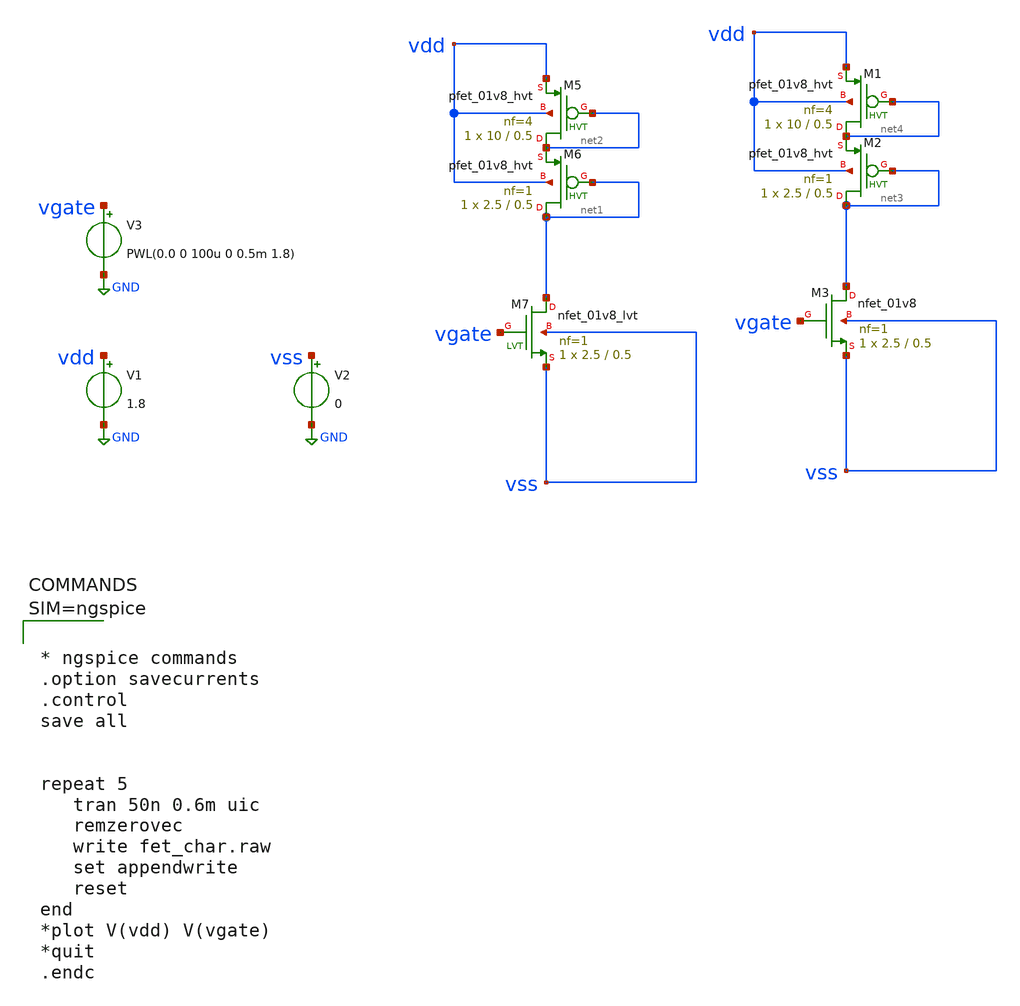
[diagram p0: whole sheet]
** sch_path: xschem/fet_char.sch
**.subckt fet_char
V1 vdd GND 1.8
V2 vss GND 0
XM5 net2 net2 vdd vdd sky130_fd_pr__pfet_01v8_hvt L=0.5 W=10 nf=4 ad='int((nf+1)/2) * W/nf * 0.29' as='int((nf+2)/2) * W/nf * 0.29'
+ pd='2*int((nf+1)/2) * (W/nf + 0.29)' ps='2*int((nf+2)/2) * (W/nf + 0.29)' nrd='0.29 / W' nrs='0.29 / W'
+ sa=0 sb=0 sd=0 mult=1 m=1
XM6 net1 net1 net2 vdd sky130_fd_pr__pfet_01v8_hvt L=0.5 W=2.5 nf=1 ad='int((nf+1)/2) * W/nf * 0.29'
+ as='int((nf+2)/2) * W/nf * 0.29' pd='2*int((nf+1)/2) * (W/nf + 0.29)' ps='2*int((nf+2)/2) * (W/nf + 0.29)'
+ nrd='0.29 / W' nrs='0.29 / W' sa=0 sb=0 sd=0 mult=1 m=1
XM7 net1 vgate vss vss sky130_fd_pr__nfet_01v8_lvt L=0.5 W=2.5 nf=1 ad='int((nf+1)/2) * W/nf * 0.29'
+ as='int((nf+2)/2) * W/nf * 0.29' pd='2*int((nf+1)/2) * (W/nf + 0.29)' ps='2*int((nf+2)/2) * (W/nf + 0.29)'
+ nrd='0.29 / W' nrs='0.29 / W' sa=0 sb=0 sd=0 mult=1 m=1
V3 vgate GND PWL(0.0 0 100u 0 0.5m 1.8)
XM1 net4 net4 vdd vdd sky130_fd_pr__pfet_01v8_hvt L=0.5 W=10 nf=4 ad='int((nf+1)/2) * W/nf * 0.29' as='int((nf+2)/2) * W/nf * 0.29'
+ pd='2*int((nf+1)/2) * (W/nf + 0.29)' ps='2*int((nf+2)/2) * (W/nf + 0.29)' nrd='0.29 / W' nrs='0.29 / W'
+ sa=0 sb=0 sd=0 mult=1 m=1
XM2 net3 net3 net4 vdd sky130_fd_pr__pfet_01v8_hvt L=0.5 W=2.5 nf=1 ad='int((nf+1)/2) * W/nf * 0.29'
+ as='int((nf+2)/2) * W/nf * 0.29' pd='2*int((nf+1)/2) * (W/nf + 0.29)' ps='2*int((nf+2)/2) * (W/nf + 0.29)'
+ nrd='0.29 / W' nrs='0.29 / W' sa=0 sb=0 sd=0 mult=1 m=1
XM3 net3 vgate vss vss sky130_fd_pr__nfet_01v8 L=0.5 W=2.5 nf=1 ad='int((nf+1)/2) * W/nf * 0.29' as='int((nf+2)/2) * W/nf * 0.29'
+ pd='2*int((nf+1)/2) * (W/nf + 0.29)' ps='2*int((nf+2)/2) * (W/nf + 0.29)' nrd='0.29 / W' nrs='0.29 / W'
+ sa=0 sb=0 sd=0 mult=1 m=1
**** begin user architecture code

** opencircuitdesign pdks install
.lib $::SKYWATER_MODELS/sky130.lib.spice tt_mm
.include $::SKYWATER_STDCELLS/sky130_fd_sc_hd.spice
.temp 27




* ngspice commands
.option savecurrents
.control
save all


repeat 5
   tran 50n 0.6m uic
   remzerovec
   write fet_char.raw
   set appendwrite
   reset
end
*plot V(vdd) V(vgate)
*quit
.endc



**** end user architecture code
**.ends
.GLOBAL GND
.end
